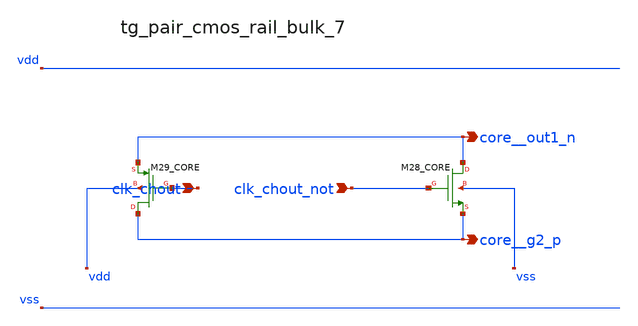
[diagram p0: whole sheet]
** sch_path: analog-db/raw/ia_006_fan_chopper_cmfb/hier/blocks/tg_pair_cmos_rail_bulk_7.sch
**.subckt tg_pair_cmos_rail_bulk_7 clk_chout clk_chout_not core__out1_n core__g2_p
*.ipin clk_chout
*.ipin clk_chout_not
*.opin core__out1_n
*.opin core__g2_p
XM28_CORE core__out1_n clk_chout_not core__g2_p vss sg13_lv_nmos w=x_dut_xm28_core_w
+ l=x_dut_xm28_core_l ng=1 m=x_dut_xm28_core_m
XM29_CORE core__g2_p clk_chout core__out1_n vdd sg13_lv_pmos w=x_dut_xm29_core_w l=x_dut_xm29_core_l
+ ng=1 m=x_dut_xm29_core_m
**.ends
.end
